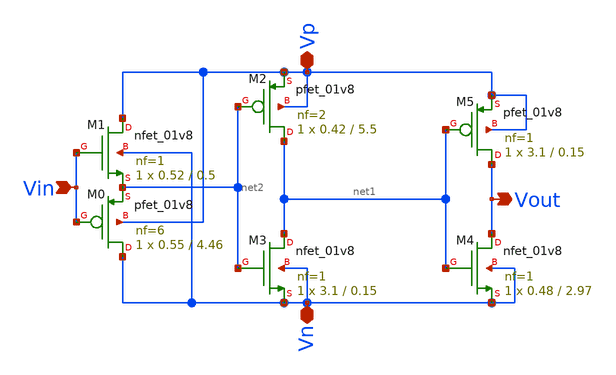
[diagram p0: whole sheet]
** sch_path: xschem/tr1/symbol/th01.sch
**.subckt th01 Vin Vout Vp Vn
*.ipin Vin
*.opin Vout
*.iopin Vp
*.iopin Vn
XM5 Vout net1 Vp Vp sky130_fd_pr__pfet_01v8 L=0.15 W=3.1 nf=1 ad='int((nf+1)/2) * W/nf * 0.29' as='int((nf+2)/2) * W/nf * 0.29'
+ pd='2*int((nf+1)/2) * (W/nf + 0.29)' ps='2*int((nf+2)/2) * (W/nf + 0.29)' nrd='0.29 / W' nrs='0.29 / W'
+ sa=0 sb=0 sd=0 mult=1 m=1
XM4 Vout net1 Vn Vn sky130_fd_pr__nfet_01v8 L=2.97 W=0.48 nf=1 ad='int((nf+1)/2) * W/nf * 0.29' as='int((nf+2)/2) * W/nf * 0.29'
+ pd='2*int((nf+1)/2) * (W/nf + 0.29)' ps='2*int((nf+2)/2) * (W/nf + 0.29)' nrd='0.29 / W' nrs='0.29 / W'
+ sa=0 sb=0 sd=0 mult=1 m=1
XM2 net1 net2 Vp Vp sky130_fd_pr__pfet_01v8 L=5.5 W=0.42 nf=2 ad='int((nf+1)/2) * W/nf * 0.29' as='int((nf+2)/2) * W/nf * 0.29'
+ pd='2*int((nf+1)/2) * (W/nf + 0.29)' ps='2*int((nf+2)/2) * (W/nf + 0.29)' nrd='0.29 / W' nrs='0.29 / W'
+ sa=0 sb=0 sd=0 mult=1 m=1
XM3 net1 net2 Vn Vn sky130_fd_pr__nfet_01v8 L=0.15 W=3.1 nf=1 ad='int((nf+1)/2) * W/nf * 0.29' as='int((nf+2)/2) * W/nf * 0.29'
+ pd='2*int((nf+1)/2) * (W/nf + 0.29)' ps='2*int((nf+2)/2) * (W/nf + 0.29)' nrd='0.29 / W' nrs='0.29 / W'
+ sa=0 sb=0 sd=0 mult=1 m=1
XM1 Vp Vin net2 Vn sky130_fd_pr__nfet_01v8 L=0.5 W=0.52 nf=1 ad='int((nf+1)/2) * W/nf * 0.29' as='int((nf+2)/2) * W/nf * 0.29'
+ pd='2*int((nf+1)/2) * (W/nf + 0.29)' ps='2*int((nf+2)/2) * (W/nf + 0.29)' nrd='0.29 / W' nrs='0.29 / W'
+ sa=0 sb=0 sd=0 mult=1 m=1
XM0 Vn Vin net2 Vp sky130_fd_pr__pfet_01v8 L=4.46 W=0.55 nf=6 ad='int((nf+1)/2) * W/nf * 0.29' as='int((nf+2)/2) * W/nf * 0.29'
+ pd='2*int((nf+1)/2) * (W/nf + 0.29)' ps='2*int((nf+2)/2) * (W/nf + 0.29)' nrd='0.29 / W' nrs='0.29 / W'
+ sa=0 sb=0 sd=0 mult=1 m=1
**.ends
.end
